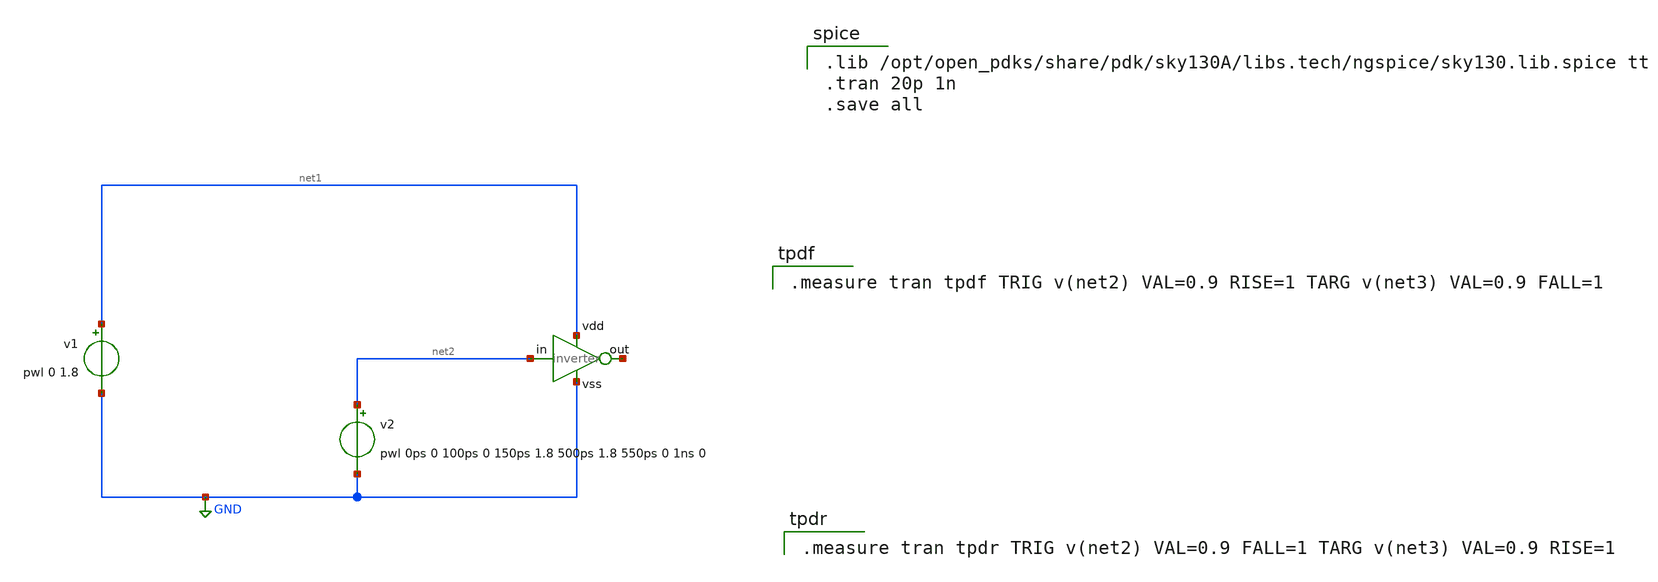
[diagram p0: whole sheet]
** sch_path: projects/carry_lookahead_adder/xschem/ports/test/rise_fall_time/inverter.sch
**.subckt inverter
v1 net1 GND pwl 0 1.8
v2 net2 GND pwl 0ps 0 100ps 0 150ps 1.8 500ps 1.8 550ps 0 1ns 0
x1 net2 net3 net1 GND inverter
**** begin user architecture code

.measure tran tpdr TRIG v(net2) VAL=0.9 FALL=1 TARG v(net3) VAL=0.9 RISE=1


.measure tran tpdf TRIG v(net2) VAL=0.9 RISE=1 TARG v(net3) VAL=0.9 FALL=1


.lib /opt/open_pdks/share/pdk/sky130A/libs.tech/ngspice/sky130.lib.spice tt
.tran 20p 1n
.save all

**** end user architecture code
**.ends

* expanding   symbol:
*+  /home/peppe/Scrivania/vlsi/circuits-simulation/projects/carry_lookahead_adder/xschem/ports/inverter.sym # of pins=4
** sym_path: projects/carry_lookahead_adder/xschem/ports/inverter.sym
** sch_path: projects/carry_lookahead_adder/xschem/ports/inverter.sch
.subckt inverter in out vdd vss
*.ipin in
*.ipin vdd
*.ipin vss
*.opin out
XM2 out in vss vss sky130_fd_pr__nfet_01v8 L=0.15 W=1 nf=1 ad='W * 0.29' as='W * 0.29' pd='W + 2 * 0.29'
+ ps='W + 2 * 0.29' nrd=0 nrs=0 sa=0 sb=0 sd=0 mult=1 m=1
XM1 out in vdd vdd sky130_fd_pr__pfet_01v8 L=0.15 W=3 nf=1 ad='W * 0.29' as='W * 0.29' pd='W + 2 * 0.29'
+ ps='W + 2 * 0.29' nrd=0 nrs=0 sa=0 sb=0 sd=0 mult=1 m=1
.ends

.GLOBAL GND
.end
